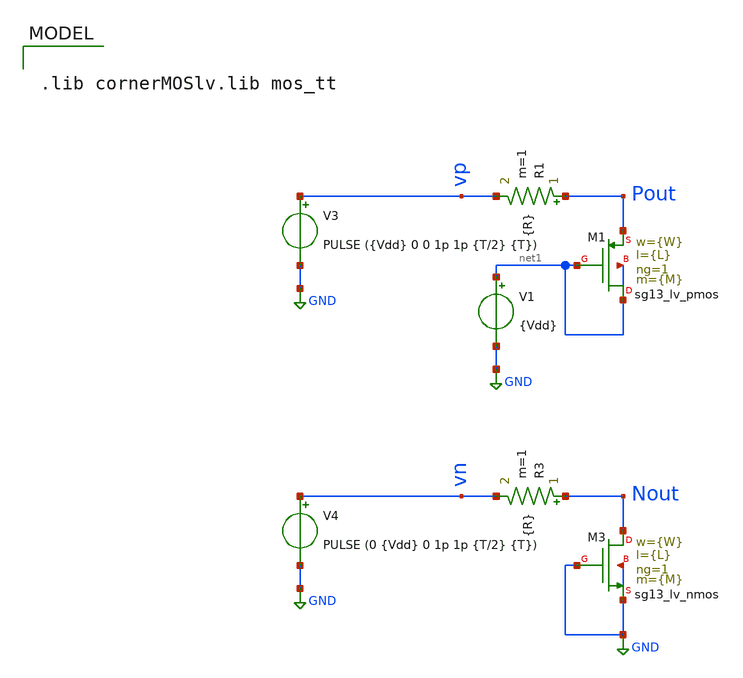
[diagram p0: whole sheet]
** sch_path: xschem/TB/TB_lvmos_Cdrain.sch
**.subckt TB_lvmos_Cdrain
R1 Pout vp {R} m=1
V3 vp GND PULSE ({Vdd} 0 0 1p 1p {T/2} {T})
V1 net1 GND {Vdd}
R3 Nout vn {R} m=1
V4 vn GND PULSE (0 {Vdd} 0 1p 1p {T/2} {T})
XM3 Nout GND GND GND sg13_lv_nmos w={W} l={L} ng=1 m={M} mm_ok=1
XM1 net1 net1 Pout net1 sg13_lv_pmos w={W} l={L} ng=1 m={M} mm_ok=1
**** begin user architecture code

.lib cornerMOSlv.lib mos_tt



.param R = 100k
.parameter T = 10n
.param Vdd = 1.0

.ic v(Pout) = 1.0
.ic v(Nout) = 0

* MOS Param
.param temp=27
.param M = 1
.param W = 0.3u
.param L = 0.13u




.control
let strt_w = 0.3u
let stop_w = 10u
let step_w = 0.1u
let curr_w = 0.3u
save all
while curr_w le stop_w
	alterparam W = $&curr_w
	reset
	tran 10p 2n
	meas tran tauN when v(Nout) = 0.63 CROSS=1
	meas tran tauP when v(Pout) = 0.37 CROSS=1
	let Cn = tauN/(100k)
	let Cp = tauP/(100k)
	wrdata ../proyecto-IPD413/simulations/Cdrain_vs_Width.raw Cn Cp curr_w
	set appendwrite
	let curr_w = curr_w + step_w
end
plot v(Nout)
.endc


**** end user architecture code
**.ends
.GLOBAL GND
.end
